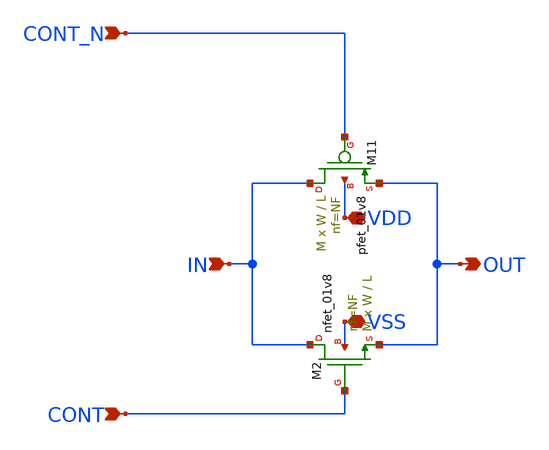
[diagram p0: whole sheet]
** sch_path: xschem/transmission_gate.sch
**.subckt transmission_gate OUT IN VDD VSS CONT CONT_N
*.opin OUT
*.ipin IN
*.iopin VDD
*.iopin VSS
*.ipin CONT
*.ipin CONT_N
XM2 IN CONT OUT VSS sky130_fd_pr__nfet_01v8 L=L W=W nf=NF ad='int((NF + 1)/2) * W / NF * 0.29' as='int((NF + 2)/2) * W / NF * 0.29'
+ pd='2*int((NF + 1)/2) * (W / NF + 0.29)' ps='2*int((NF + 2)/2) * (W / NF + 0.29)' nrd='0.29 / W ' nrs='0.29 / W '
+ sa=0 sb=0 sd=0 mult=M m=M
XM11 IN CONT_N OUT VDD sky130_fd_pr__pfet_01v8 L=L W=W nf=NF ad='int((nf+1)/2) * W/nf * 0.29' as='int((nf+2)/2) * W/nf * 0.29'
+ pd='2*int((nf+1)/2) * (W/nf + 0.29)' ps='2*int((nf+2)/2) * (W/nf + 0.29)' nrd='0.29 / W' nrs='0.29 / W'
+ sa=0 sb=0 sd=0 mult=M m=M
**.ends
.end
